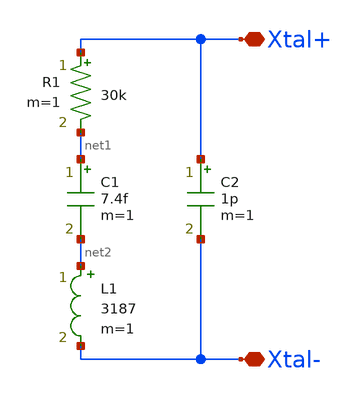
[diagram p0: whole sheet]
** sch_path: design/THESIS_EXP_RO_INVERTER_SKY130A/easy_xtal.sch
**.subckt easy_xtal Xtal+ Xtal-
*.iopin Xtal+
*.iopin Xtal-
R1 Xtal+ net1 30k m=1
C1 net1 net2 7.4f m=1
L1 net2 Xtal- 3187 m=1
C2 Xtal+ Xtal- 1p m=1
**.ends
.end
